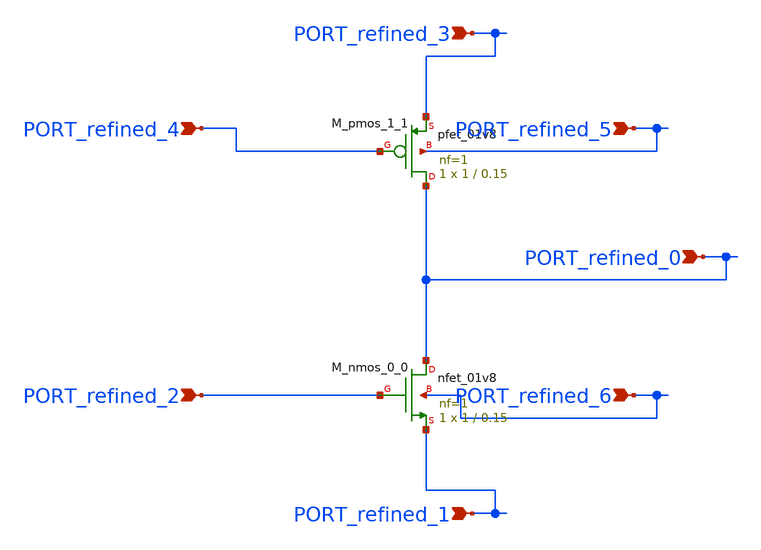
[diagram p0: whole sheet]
** sch_path: schematics/AMSNet/186.sch
**.subckt 186 PORT_refined_2 PORT_refined_4 PORT_refined_0 PORT_refined_3 PORT_refined_1
*+ PORT_refined_5 PORT_refined_6
*.ipin PORT_refined_2
*.ipin PORT_refined_4
*.ipin PORT_refined_0
*.ipin PORT_refined_3
*.ipin PORT_refined_1
*.ipin PORT_refined_5
*.ipin PORT_refined_6
XM_nmos_0_0 PORT_refined_0 PORT_refined_2 PORT_refined_1 PORT_refined_6 sky130_fd_pr__nfet_01v8 L=0.15
+ W=1 nf=1 ad='int((1 + 1)/2) * 1 / 1 * 0.29' as='int((1 + 2)/2) * 1 / 1 * 0.29' pd='2*int((1 + 1)/2) * (1 / 1 + 0.29)'
+ ps='2*int((1 + 2)/2) * (1 / 1 + 0.29)' nrd='0.29 / 1 ' nrs='0.29 / 1 ' sa=0 sb=0 sd=0 mult=1 m=1
XM_pmos_1_1 PORT_refined_0 PORT_refined_4 PORT_refined_3 PORT_refined_5 sky130_fd_pr__pfet_01v8 L=0.15
+ W=1 nf=1 ad='int((1 + 1)/2) * 1 / 1 * 0.29' as='int((1 + 2)/2) * 1 / 1 * 0.29' pd='2*int((1 + 1)/2) * (1 / 1 + 0.29)'
+ ps='2*int((1 + 2)/2) * (1 / 1 + 0.29)' nrd='0.29 / 1 ' nrs='0.29 / 1 ' sa=0 sb=0 sd=0 mult=1 m=1
**.ends
.end
